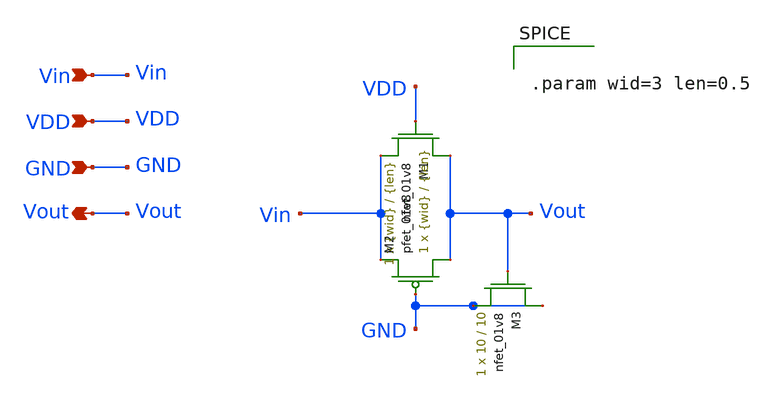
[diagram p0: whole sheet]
** sch_path: final/schematics/voltage_buffer.sch
**.subckt voltage_buffer Vin VDD GND Vout
*.ipin Vin
*.ipin VDD
*.ipin GND
*.opin Vout
XM1 Vout VDD Vin GND sky130_fd_pr__nfet_01v8 L={len} W={wid} nf=1 ad='int((nf+1)/2) * W/nf * 0.29' as='int((nf+2)/2) * W/nf * 0.29'
+ pd='2*int((nf+1)/2) * (W/nf + 0.29)' ps='2*int((nf+2)/2) * (W/nf + 0.29)' nrd='0.29 / W' nrs='0.29 / W'
+ sa=0 sb=0 sd=0 mult=1 m=1
XM2 Vout GND Vin VDD sky130_fd_pr__pfet_01v8 L={len} W={wid} nf=1 ad='int((nf+1)/2) * W/nf * 0.29' as='int((nf+2)/2) * W/nf * 0.29'
+ pd='2*int((nf+1)/2) * (W/nf + 0.29)' ps='2*int((nf+2)/2) * (W/nf + 0.29)' nrd='0.29 / W' nrs='0.29 / W'
+ sa=0 sb=0 sd=0 mult=1 m=1
XM3 GND Vout GND GND sky130_fd_pr__nfet_01v8 L=10 W=10 nf=1 ad='int((nf+1)/2) * W/nf * 0.29' as='int((nf+2)/2) * W/nf * 0.29'
+ pd='2*int((nf+1)/2) * (W/nf + 0.29)' ps='2*int((nf+2)/2) * (W/nf + 0.29)' nrd='0.29 / W' nrs='0.29 / W'
+ sa=0 sb=0 sd=0 mult=1 m=1
**** begin user architecture code


.param wid=3 len=0.5


**** end user architecture code
**.ends
.end
